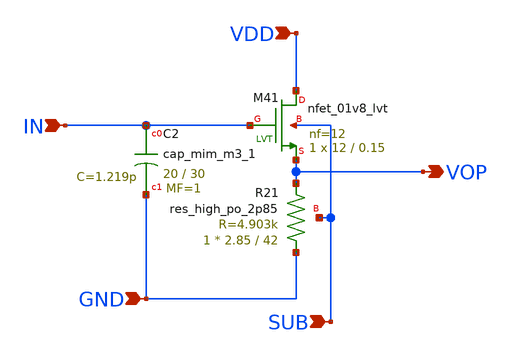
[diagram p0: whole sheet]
** sch_path: design/vco/5~10Ghiarachy_final/vop_dec.sch
**.subckt vop_dec IN VDD GND SUB VOP
*.ipin IN
*.ipin VDD
*.ipin GND
*.ipin SUB
*.opin VOP
XM41 VDD IN VOP SUB sky130_fd_pr__nfet_01v8_lvt L=0.15 W=12 nf=12 ad='int((nf+1)/2) * W/nf * 0.29' as='int((nf+2)/2) * W/nf * 0.29'
+ pd='2*int((nf+1)/2) * (W/nf + 0.29)' ps='2*int((nf+2)/2) * (W/nf + 0.29)' nrd='0.29 / W' nrs='0.29 / W'
+ sa=0 sb=0 sd=0 mult=1 m=1
XC2 IN GND sky130_fd_pr__cap_mim_m3_1 W=20 L=30 MF=1 m=1
XR21 GND VOP SUB sky130_fd_pr__res_high_po_2p85 L=42 mult=1 m=1
**.ends
.end
